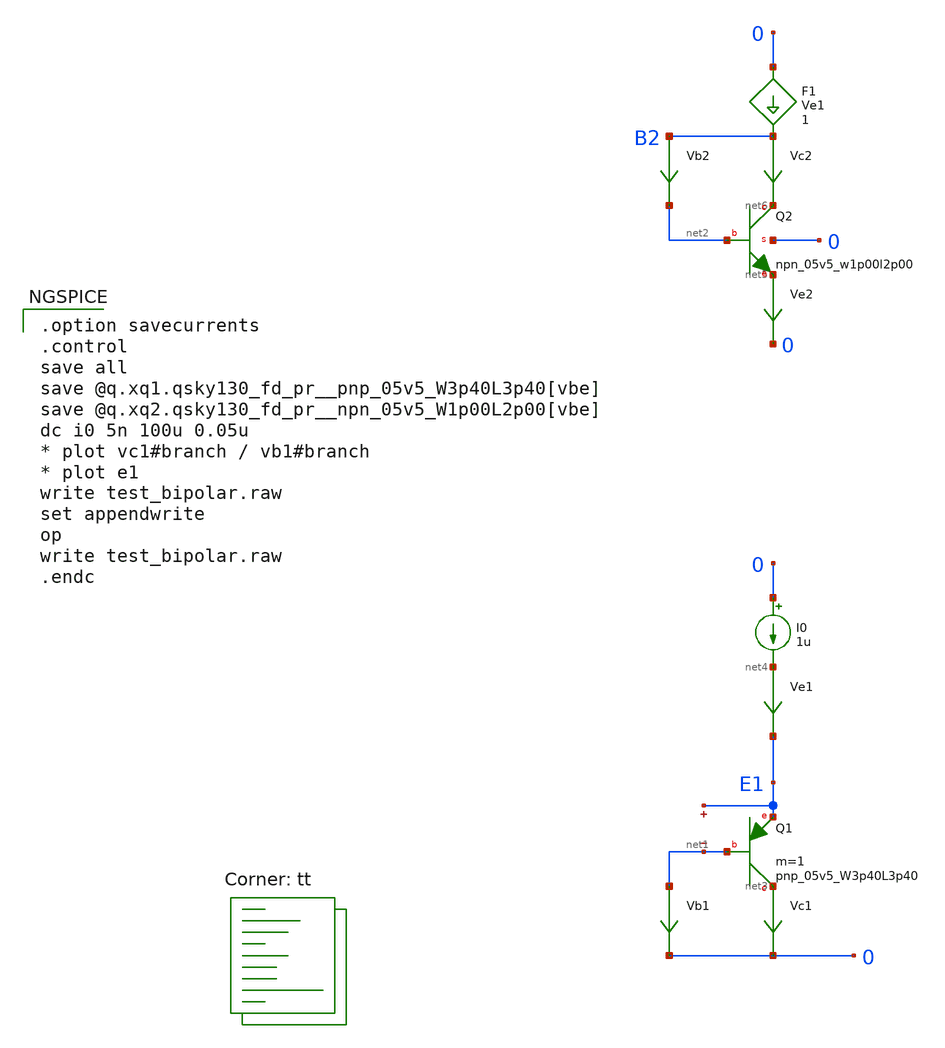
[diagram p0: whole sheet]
** sch_path: sky130A/xschem_libs/sky130_tests/test_bipolar/schematic/test_bipolar.sch
* Copyright 2021 Stefan Frederik Schippers
* Licensed under the Apache License, Version 2.0 (the "License");
* you may not use this file except in compliance with the License.
* You may obtain a copy of the License at
* https://www.apache.org/licenses/LICENSE-2.0
* Unless required by applicable law or agreed to in writing, software
* distributed under the License is distributed on an "AS IS" BASIS,
* WITHOUT WARRANTIES OR CONDITIONS OF ANY KIND, either express or implied.
* See the License for the specific language governing permissions and
* limitations under the License.
**.subckt test_bipolar
XQ1 net3 net1 E1 sky130_fd_pr__pnp_05v5_W3p40L3p40 m=1
Vc1 net3 0 0
.save i(vc1)
Vb1 net1 0 0
.save i(vb1)
I0 0 net4 1u
Ve1 net4 E1 0
.save i(ve1)
.save v(e1)
.save v(net1)
Ve2 net5 0 0
.save i(ve2)
Vc2 B2 net6 0
.save i(vc2)
Vb2 B2 net2 0
.save i(vb2)
XQ2 net6 net2 net5 0 sky130_fd_pr__npn_05v5_w1p00l2p00
F1 0 B2 Ve1 1
**** begin user architecture code

.option savecurrents
.control
save all
save @q.xq1.qsky130_fd_pr__pnp_05v5_W3p40L3p40[vbe]
save @q.xq2.qsky130_fd_pr__npn_05v5_W1p00L2p00[vbe]
dc i0 5n 100u 0.05u
* plot vc1#branch / vb1#branch
* plot e1
write test_bipolar.raw
set appendwrite
op
write test_bipolar.raw
.endc


.lib $::SKYWATER_MODELS/sky130.lib.spice tt
**** end user architecture code
**.ends
.end
